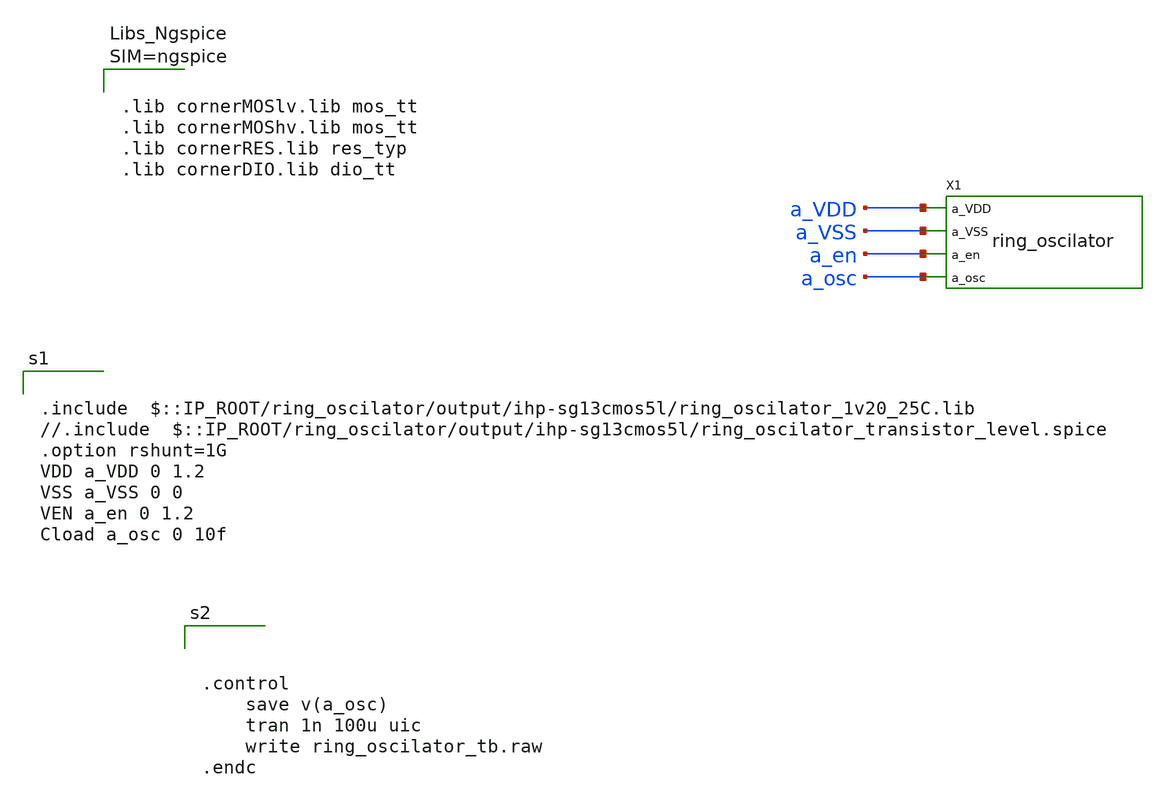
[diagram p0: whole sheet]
** sch_path: ring_oscilator/ring_oscilator_tb.sch
**.subckt ring_oscilator_tb
X1 a_VDD a_VSS a_en a_osc ring_oscilator
**** begin user architecture code

.include  $::IP_ROOT/ring_oscilator/output/ihp-sg13cmos5l/ring_oscilator_1v20_25C.lib
//.include  $::IP_ROOT/ring_oscilator/output/ihp-sg13cmos5l/ring_oscilator_transistor_level.spice
.option rshunt=1G
VDD a_VDD 0 1.2
VSS a_VSS 0 0
VEN a_en 0 1.2
Cload a_osc 0 10f





.control
	save v(a_osc)
	tran 1n 100u uic
	write ring_oscilator_tb.raw
.endc






.lib cornerMOSlv.lib mos_tt
.lib cornerMOShv.lib mos_tt
.lib cornerRES.lib res_typ
.lib cornerDIO.lib dio_tt



**** end user architecture code
**.ends
.end
